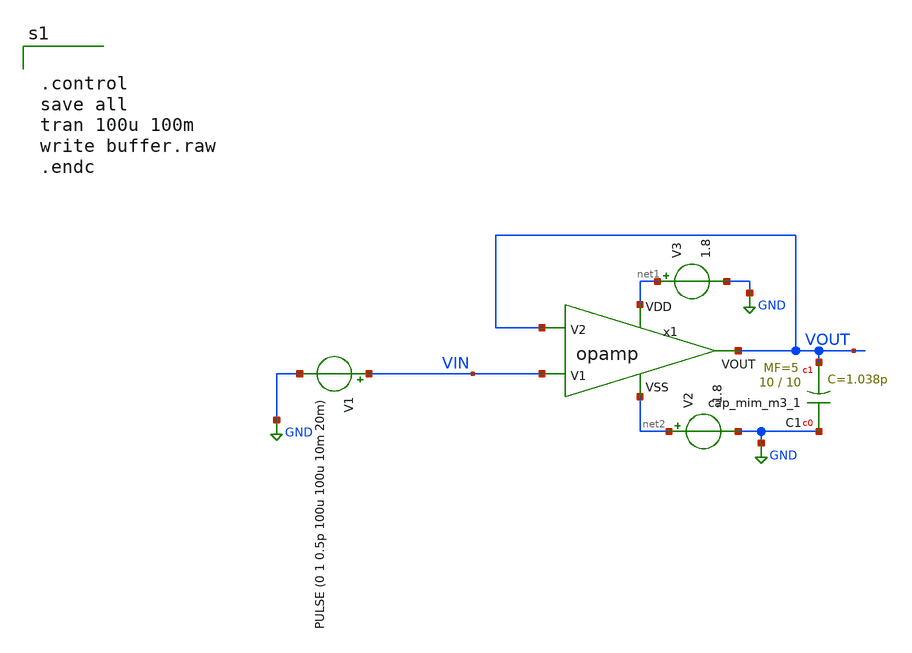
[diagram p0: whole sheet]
** sch_path: slew_rate.sch
**.subckt slew_rate
V3 net1 GND 1.8
V2 net2 GND -1.8
V1 VIN GND PULSE (0 1 0.5p 100u 100u 10m 20m)
x1 net1 VOUT VIN VOUT net2 opamp
XC1 GND VOUT sky130_fd_pr__cap_mim_m3_1 W=10 L=10 MF=5 m=5
**** begin user architecture code

** opencircuitdesign pdks install
.lib $::SKYWATER_MODELS/sky130.lib.spice tt




.control
save all
tran 100u 100m
write buffer.raw
.endc


**** end user architecture code
**.ends

* expanding   symbol:  /foss/designs/FINAL_PROJECT_KTMDT/opamp.sym # of pins=5
** sym_path: /foss/designs/FINAL_PROJECT_KTMDT/opamp.sym
** sch_path: /foss/designs/FINAL_PROJECT_KTMDT/opamp.sch
.subckt opamp VDD V2 V1 VOUT VSS
*.ipin VSS
*.ipin VDD
*.ipin V2
*.ipin V1
*.opin VOUT
XM3 net4 V2 net1 VSS sky130_fd_pr__nfet_g5v0d10v5 L=1 W=17.45 nf=1 ad='int((nf+1)/2) * W/nf * 0.29' as='int((nf+2)/2) * W/nf * 0.29'
+ pd='2*int((nf+1)/2) * (W/nf + 0.29)' ps='2*int((nf+2)/2) * (W/nf + 0.29)' nrd='0.29 / W' nrs='0.29 / W'
+ sa=0 sb=0 sd=0 mult=1 m=1
XM1 net5 net4 VDD VDD sky130_fd_pr__pfet_g5v0d10v5 L=1 W=30 nf=1 ad='int((nf+1)/2) * W/nf * 0.29' as='int((nf+2)/2) * W/nf * 0.29'
+ pd='2*int((nf+1)/2) * (W/nf + 0.29)' ps='2*int((nf+2)/2) * (W/nf + 0.29)' nrd='0.29 / W' nrs='0.29 / W'
+ sa=0 sb=0 sd=0 mult=1 m=1
XM4 net5 V1 net1 VSS sky130_fd_pr__nfet_g5v0d10v5 L=1 W=17.45 nf=1 ad='int((nf+1)/2) * W/nf * 0.29' as='int((nf+2)/2) * W/nf * 0.29'
+ pd='2*int((nf+1)/2) * (W/nf + 0.29)' ps='2*int((nf+2)/2) * (W/nf + 0.29)' nrd='0.29 / W' nrs='0.29 / W'
+ sa=0 sb=0 sd=0 mult=1 m=1
XM6 net1 net6 VSS VSS sky130_fd_pr__nfet_g5v0d10v5 L=1 W=15.17 nf=1 ad='int((nf+1)/2) * W/nf * 0.29'
+ as='int((nf+2)/2) * W/nf * 0.29' pd='2*int((nf+1)/2) * (W/nf + 0.29)' ps='2*int((nf+2)/2) * (W/nf + 0.29)'
+ nrd='0.29 / W' nrs='0.29 / W' sa=0 sb=0 sd=0 mult=1 m=1
XM7 VOUT net6 VSS VSS sky130_fd_pr__nfet_g5v0d10v5 L=1 W=19 nf=1 ad='int((nf+1)/2) * W/nf * 0.29' as='int((nf+2)/2) * W/nf * 0.29'
+ pd='2*int((nf+1)/2) * (W/nf + 0.29)' ps='2*int((nf+2)/2) * (W/nf + 0.29)' nrd='0.29 / W' nrs='0.29 / W'
+ sa=0 sb=0 sd=0 mult=1 m=1
XM5 net6 net6 VSS VSS sky130_fd_pr__nfet_g5v0d10v5 L=1 W=15.17 nf=1 ad='int((nf+1)/2) * W/nf * 0.29'
+ as='int((nf+2)/2) * W/nf * 0.29' pd='2*int((nf+1)/2) * (W/nf + 0.29)' ps='2*int((nf+2)/2) * (W/nf + 0.29)'
+ nrd='0.29 / W' nrs='0.29 / W' sa=0 sb=0 sd=0 mult=1 m=1
XM2 net4 net4 VDD VDD sky130_fd_pr__pfet_g5v0d10v5 L=1 W=30 nf=1 ad='int((nf+1)/2) * W/nf * 0.29' as='int((nf+2)/2) * W/nf * 0.29'
+ pd='2*int((nf+1)/2) * (W/nf + 0.29)' ps='2*int((nf+2)/2) * (W/nf + 0.29)' nrd='0.29 / W' nrs='0.29 / W'
+ sa=0 sb=0 sd=0 mult=1 m=1
XM8 VOUT net5 VDD VDD sky130_fd_pr__pfet_g5v0d10v5 L=1 W=38 nf=1 ad='int((nf+1)/2) * W/nf * 0.29' as='int((nf+2)/2) * W/nf * 0.29'
+ pd='2*int((nf+1)/2) * (W/nf + 0.29)' ps='2*int((nf+2)/2) * (W/nf + 0.29)' nrd='0.29 / W' nrs='0.29 / W'
+ sa=0 sb=0 sd=0 mult=2 m=2
V_ibias net7 net6 0
.save i(v_ibias)
XR1 net2 VDD VSS sky130_fd_pr__res_high_po W=1 L=41.1 mult=1 m=1
XR2 net3 net2 VSS sky130_fd_pr__res_high_po W=1 L=41.1 mult=1 m=1
XR3 net7 net3 VSS sky130_fd_pr__res_high_po W=1 L=41.1 mult=1 m=1
XR4 net8 VOUT VSS sky130_fd_pr__res_high_po W=1 L=5 mult=1 m=1
XC1 net8 net5 sky130_fd_pr__cap_mim_m3_1 W=9 L=9 MF=2 m=2
.ends

.GLOBAL GND
.end
